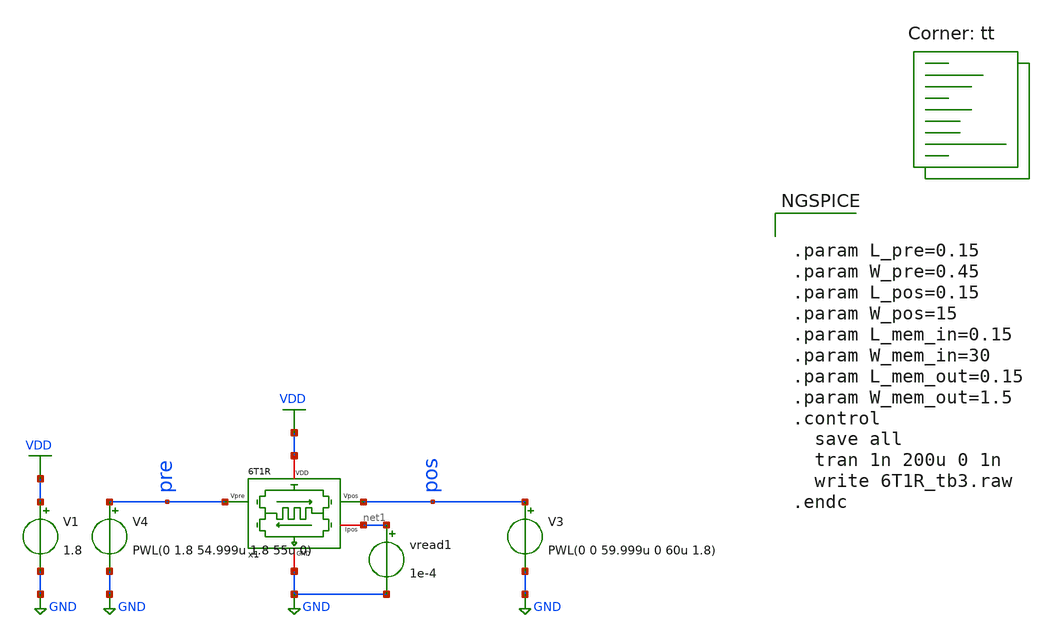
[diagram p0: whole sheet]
** sch_path: synapse/6T1R_tb.sch
**.subckt 6T1R_tb
V1 VDD GND 1.8
V3 pos GND PWL(0 0 59.999u 0 60u 1.8)
vread1 net1 GND 1e-4
x1 VDD net1 pre pos GND 6T1R
V4 pre GND PWL(0 1.8 54.999u 1.8 55u 0)
**** begin user architecture code
.lib $::SKYWATER_MODELS/sky130.lib.spice tt

** opencircuitdesign pdks install
.inc $::SKYWATER_MODELS/rram_v0.spice
.inc $::SKYWATER_MODELS/rram_v1.spice



.param L_pre=0.15
.param W_pre=0.45
.param L_pos=0.15
.param W_pos=15
.param L_mem_in=0.15
.param W_mem_in=30
.param L_mem_out=0.15
.param W_mem_out=1.5
.control
  save all
  tran 1n 200u 0 1n
  write 6T1R_tb3.raw
.endc


**** end user architecture code
**.ends

* expanding   symbol:  /home/ricardo/RATT_repos/Proyectos_xschem/synapse/6T1R.sym # of pins=5
** sym_path: synapse/6T1R.sym
** sch_path: synapse/6T1R.sch
.subckt 6T1R VDD Ipos Vpre Vpos GND
*.ipin Vpre
*.ipin Vpos
*.iopin GND
*.iopin Ipos
*.iopin VDD
XM1 vipre Vpre net1 GND sky130_fd_pr__nfet_01v8 L=0.15 W=10 nf=1 ad='int((nf+1)/2) * W/nf * 0.29' as='int((nf+2)/2) * W/nf * 0.29'
+ pd='2*int((nf+1)/2) * (W/nf + 0.29)' ps='2*int((nf+2)/2) * (W/nf + 0.29)' nrd='0.29 / W' nrs='0.29 / W'
+ sa=0 sb=0 sd=0 mult=1 m=1
XR1 net2 net1 rram_v0
XM3 vipre Vpos net2 GND sky130_fd_pr__nfet_01v8 L=0.15 W=1 nf=1 ad='int((nf+1)/2) * W/nf * 0.29' as='int((nf+2)/2) * W/nf * 0.29'
+ pd='2*int((nf+1)/2) * (W/nf + 0.29)' ps='2*int((nf+2)/2) * (W/nf + 0.29)' nrd='0.29 / W' nrs='0.29 / W'
+ sa=0 sb=0 sd=0 mult=1 m=1
XM6 Ipos vipre VDD VDD sky130_fd_pr__pfet_01v8 L=0.15 W=1 nf=1 ad='int((nf+1)/2) * W/nf * 0.29' as='int((nf+2)/2) * W/nf * 0.29'
+ pd='2*int((nf+1)/2) * (W/nf + 0.29)' ps='2*int((nf+2)/2) * (W/nf + 0.29)' nrd='0.29 / W' nrs='0.29 / W'
+ sa=0 sb=0 sd=0 mult=1 m=1
XM5 vipre vipre VDD VDD sky130_fd_pr__pfet_01v8 L=0.15 W=20 nf=1 ad='int((nf+1)/2) * W/nf * 0.29' as='int((nf+2)/2) * W/nf * 0.29'
+ pd='2*int((nf+1)/2) * (W/nf + 0.29)' ps='2*int((nf+2)/2) * (W/nf + 0.29)' nrd='0.29 / W' nrs='0.29 / W'
+ sa=0 sb=0 sd=0 mult=1 m=1
XM2 net1 Vpos GND GND sky130_fd_pr__nfet_01v8 L=0.15 W=1 nf=1 ad='int((nf+1)/2) * W/nf * 0.29' as='int((nf+2)/2) * W/nf * 0.29'
+ pd='2*int((nf+1)/2) * (W/nf + 0.29)' ps='2*int((nf+2)/2) * (W/nf + 0.29)' nrd='0.29 / W' nrs='0.29 / W'
+ sa=0 sb=0 sd=0 mult=1 m=1
XM4 net2 Vpre GND GND sky130_fd_pr__nfet_01v8 L=0.15 W=10 nf=1 ad='int((nf+1)/2) * W/nf * 0.29' as='int((nf+2)/2) * W/nf * 0.29'
+ pd='2*int((nf+1)/2) * (W/nf + 0.29)' ps='2*int((nf+2)/2) * (W/nf + 0.29)' nrd='0.29 / W' nrs='0.29 / W'
+ sa=0 sb=0 sd=0 mult=1 m=1
.ends

.GLOBAL GND
.GLOBAL VDD
.end
